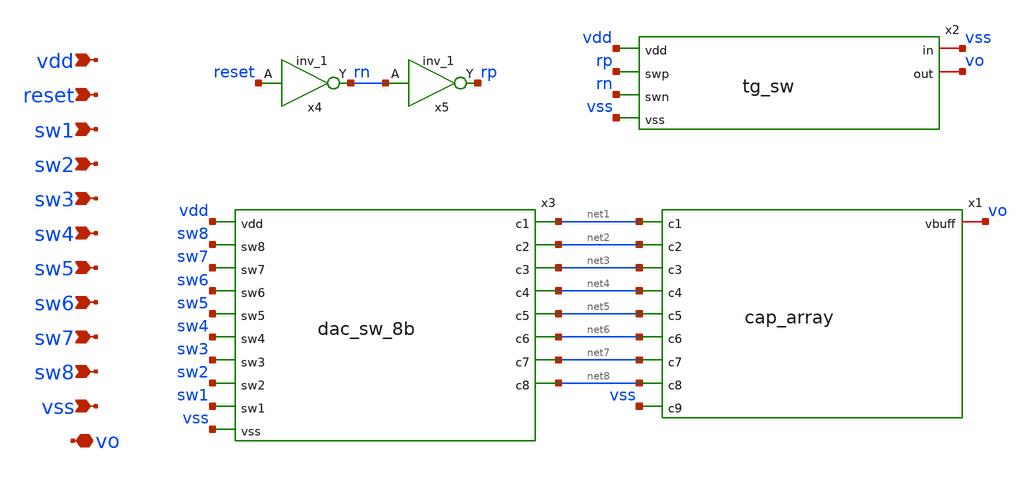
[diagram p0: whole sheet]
** sch_path: xschem/dac_8b.sch
**.subckt dac_8b vdd reset sw1 sw2 sw3 sw4 sw5 sw6 sw7 sw8 vss vo
*.ipin vdd
*.ipin reset
*.ipin sw1
*.ipin sw2
*.ipin sw3
*.ipin sw4
*.ipin sw5
*.ipin sw6
*.ipin sw7
*.ipin sw8
*.ipin vss
*.iopin vo
x1 net1 net2 net3 net4 net5 net6 net7 net8 vss vo cap_array
x3 vdd sw8 sw7 net1 net2 sw6 sw5 net3 sw4 net4 net5 sw3 net6 sw2 net7 sw1 net8 vss dac_sw_8b
x4 reset vss vss vdd vdd rn sky130_fd_sc_hd__inv_1
x5 rn vss vss vdd vdd rp sky130_fd_sc_hd__inv_1
x2 vdd rp rn vss vss vo tg_sw
**.ends

* expanding   symbol:  /home/mthudaa/Documents/Time_SAR_ADC/xschem/cap_array.sym # of pins=10
** sym_path: xschem/cap_array.sym
** sch_path: xschem/cap_array.sch
.subckt cap_array c1 c2 c3 c4 c5 c6 c7 c8 c9 vbuff
*.ipin c1
*.ipin c2
*.ipin c3
*.ipin c4
*.ipin c5
*.ipin c6
*.ipin c7
*.ipin c8
*.ipin c9
*.iopin vbuff
XC1 vbuff c9 sky130_fd_pr__cap_mim_m3_1 W=1 L=1 MF=1 m=1
XC2 vbuff c8 sky130_fd_pr__cap_mim_m3_1 W=1 L=1 MF=1 m=1
XC3 vbuff c7 sky130_fd_pr__cap_mim_m3_1 W=1 L=1 MF=2 m=2
XC4 vbuff c6 sky130_fd_pr__cap_mim_m3_1 W=1 L=1 MF=4 m=4
XC5 vbuff c5 sky130_fd_pr__cap_mim_m3_1 W=1 L=1 MF=8 m=8
XC6 vbuff c4 sky130_fd_pr__cap_mim_m3_1 W=1 L=1 MF=16 m=16
XC7 vbuff c3 sky130_fd_pr__cap_mim_m3_1 W=1 L=1 MF=32 m=32
XC8 vbuff c2 sky130_fd_pr__cap_mim_m3_1 W=1 L=1 MF=64 m=64
XC9 vbuff c1 sky130_fd_pr__cap_mim_m3_1 W=1 L=1 MF=128 m=128
.ends


* expanding   symbol:  /home/mthudaa/Documents/Time_SAR_ADC/xschem/dac_sw_8b.sym # of pins=18
** sym_path: xschem/dac_sw_8b.sym
** sch_path: xschem/dac_sw_8b.sch
.subckt dac_sw_8b vdd sw8 sw7 c1 c2 sw6 sw5 c3 sw4 c4 c5 sw3 c6 sw2 c7 sw1 c8 vss
*.ipin vdd
*.ipin sw8
*.ipin sw7
*.ipin sw6
*.ipin sw5
*.ipin sw4
*.ipin sw3
*.ipin sw2
*.ipin sw1
*.ipin vss
*.opin c8
*.opin c7
*.opin c6
*.opin c5
*.opin c4
*.opin c3
*.opin c2
*.opin c1
x9 sw8 vss vss vdd vdd sky130_fd_sc_hd__diode_2
x10 sw7 vss vss vdd vdd sky130_fd_sc_hd__diode_2
x11 sw6 vss vss vdd vdd sky130_fd_sc_hd__diode_2
x12 sw5 vss vss vdd vdd sky130_fd_sc_hd__diode_2
x13 sw4 vss vss vdd vdd sky130_fd_sc_hd__diode_2
x14 sw3 vss vss vdd vdd sky130_fd_sc_hd__diode_2
x15 sw2 vss vss vdd vdd sky130_fd_sc_hd__diode_2
x16 sw1 vss vss vdd vdd sky130_fd_sc_hd__diode_2
x1 sw8 vss vss vdd vdd c8 sky130_fd_sc_hd__clkinv_16
x2 sw7 vss vss vdd vdd c7 sky130_fd_sc_hd__clkinv_16
x3 sw6 vss vss vdd vdd c6 sky130_fd_sc_hd__clkinv_16
x4 sw5 vss vss vdd vdd c5 sky130_fd_sc_hd__clkinv_16
x5 sw4 vss vss vdd vdd c4 sky130_fd_sc_hd__clkinv_16
x6 sw3 vss vss vdd vdd c3 sky130_fd_sc_hd__clkinv_16
x7 sw2 vss vss vdd vdd c2 sky130_fd_sc_hd__clkinv_16
x8 sw1 vss vss vdd vdd c1 sky130_fd_sc_hd__clkinv_16
.ends


* expanding   symbol:  /home/mthudaa/Documents/Time_SAR_ADC/xschem/tg_sw.sym # of pins=6
** sym_path: xschem/tg_sw.sym
** sch_path: xschem/tg_sw.sch
.subckt tg_sw vdd swp swn vss in out
*.ipin vdd
*.ipin swp
*.ipin swn
*.ipin vss
*.iopin in
*.iopin out
XM1 in swp out vss sky130_fd_pr__nfet_01v8 L=0.15 W=1 nf=1 ad='int((nf+1)/2) * W/nf * 0.29' as='int((nf+2)/2) * W/nf * 0.29'
+ pd='2*int((nf+1)/2) * (W/nf + 0.29)' ps='2*int((nf+2)/2) * (W/nf + 0.29)' nrd='0.29 / W' nrs='0.29 / W'
+ sa=0 sb=0 sd=0 mult=1 m=1
XM2 in swn out vdd sky130_fd_pr__pfet_01v8 L=0.15 W=1.5 nf=1 ad='int((nf+1)/2) * W/nf * 0.29' as='int((nf+2)/2) * W/nf * 0.29'
+ pd='2*int((nf+1)/2) * (W/nf + 0.29)' ps='2*int((nf+2)/2) * (W/nf + 0.29)' nrd='0.29 / W' nrs='0.29 / W'
+ sa=0 sb=0 sd=0 mult=1 m=1
.ends

.end
